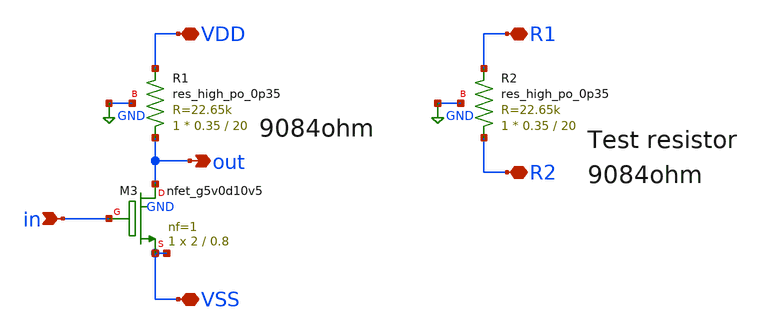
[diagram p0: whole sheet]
** sch_path: xschem/cellA.sch
**.subckt cellA in VDD out VSS R1 R2
*.ipin in
*.iopin VDD
*.opin out
*.iopin VSS
*.iopin R1
*.iopin R2
XM3 out in VSS GND sky130_fd_pr__nfet_g5v0d10v5 L=0.8 W=2 nf=1 ad='int((nf+1)/2) * W/nf * 0.29' as='int((nf+2)/2) * W/nf * 0.29'
+ pd='2*int((nf+1)/2) * (W/nf + 0.29)' ps='2*int((nf+2)/2) * (W/nf + 0.29)' nrd='0.29 / W' nrs='0.29 / W'
+ sa=0 sb=0 sd=0 mult=1 m=1
XR1 out VDD GND sky130_fd_pr__res_high_po_0p35 L=20 mult=1 m=1
XR2 R2 R1 GND sky130_fd_pr__res_high_po_0p35 L=20 mult=1 m=1
**.ends
.GLOBAL GND
.end
